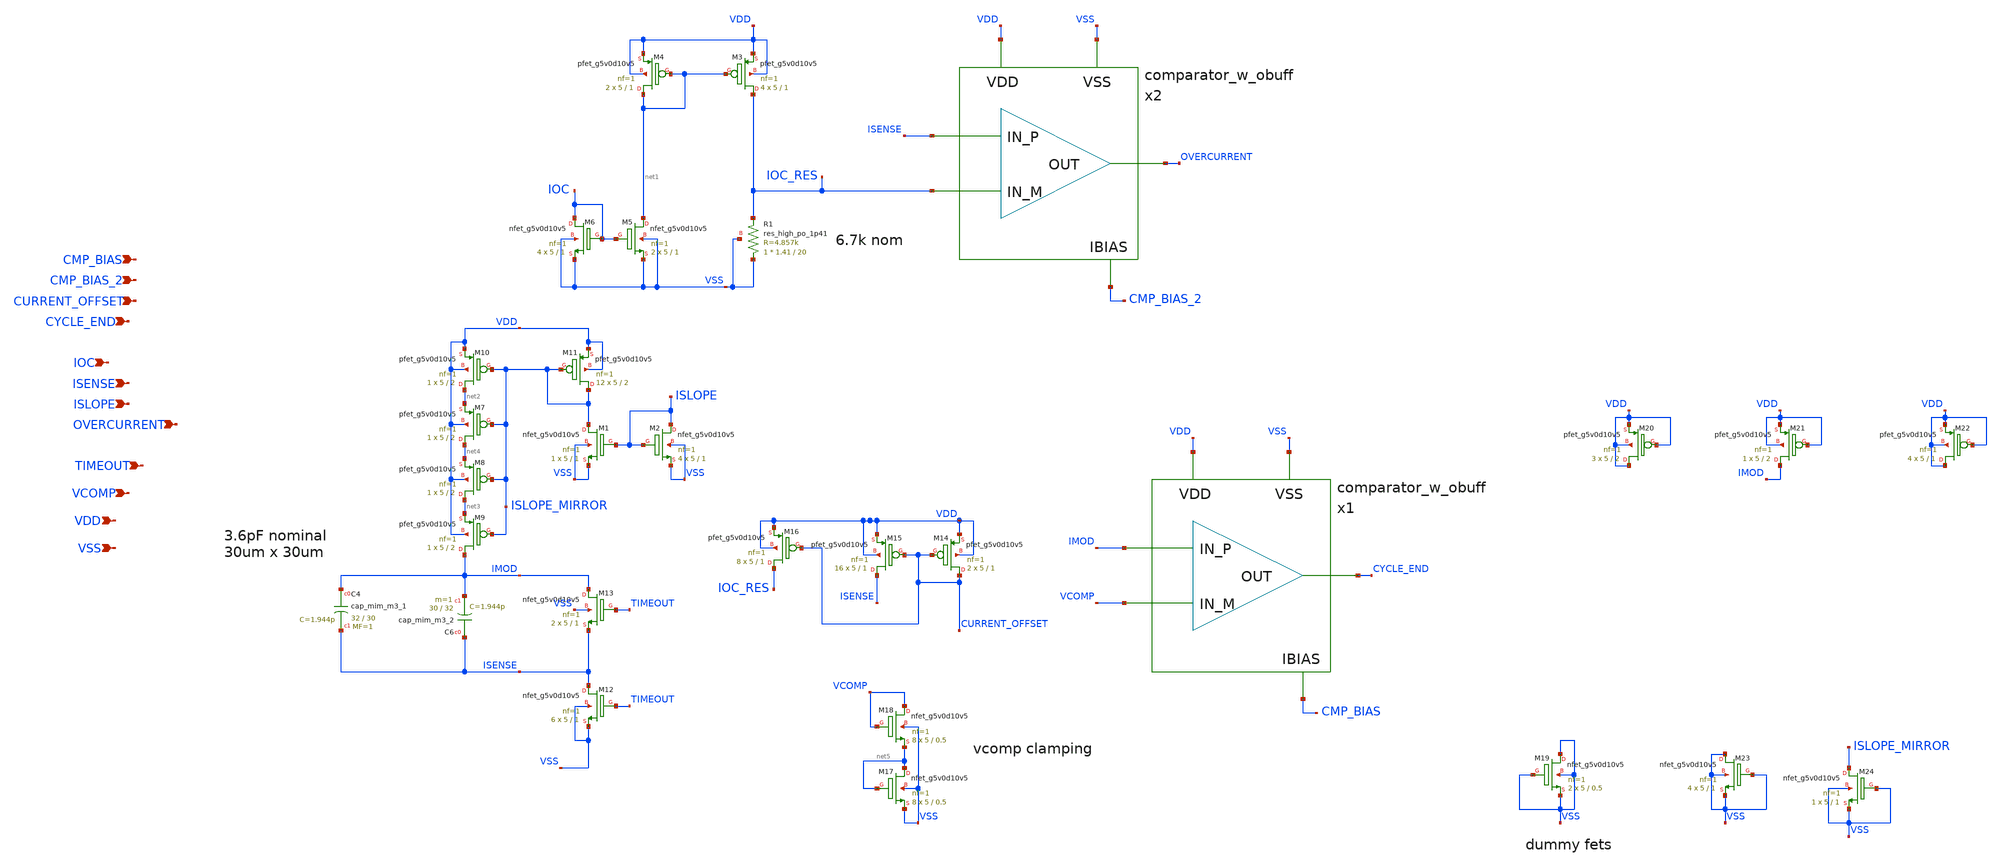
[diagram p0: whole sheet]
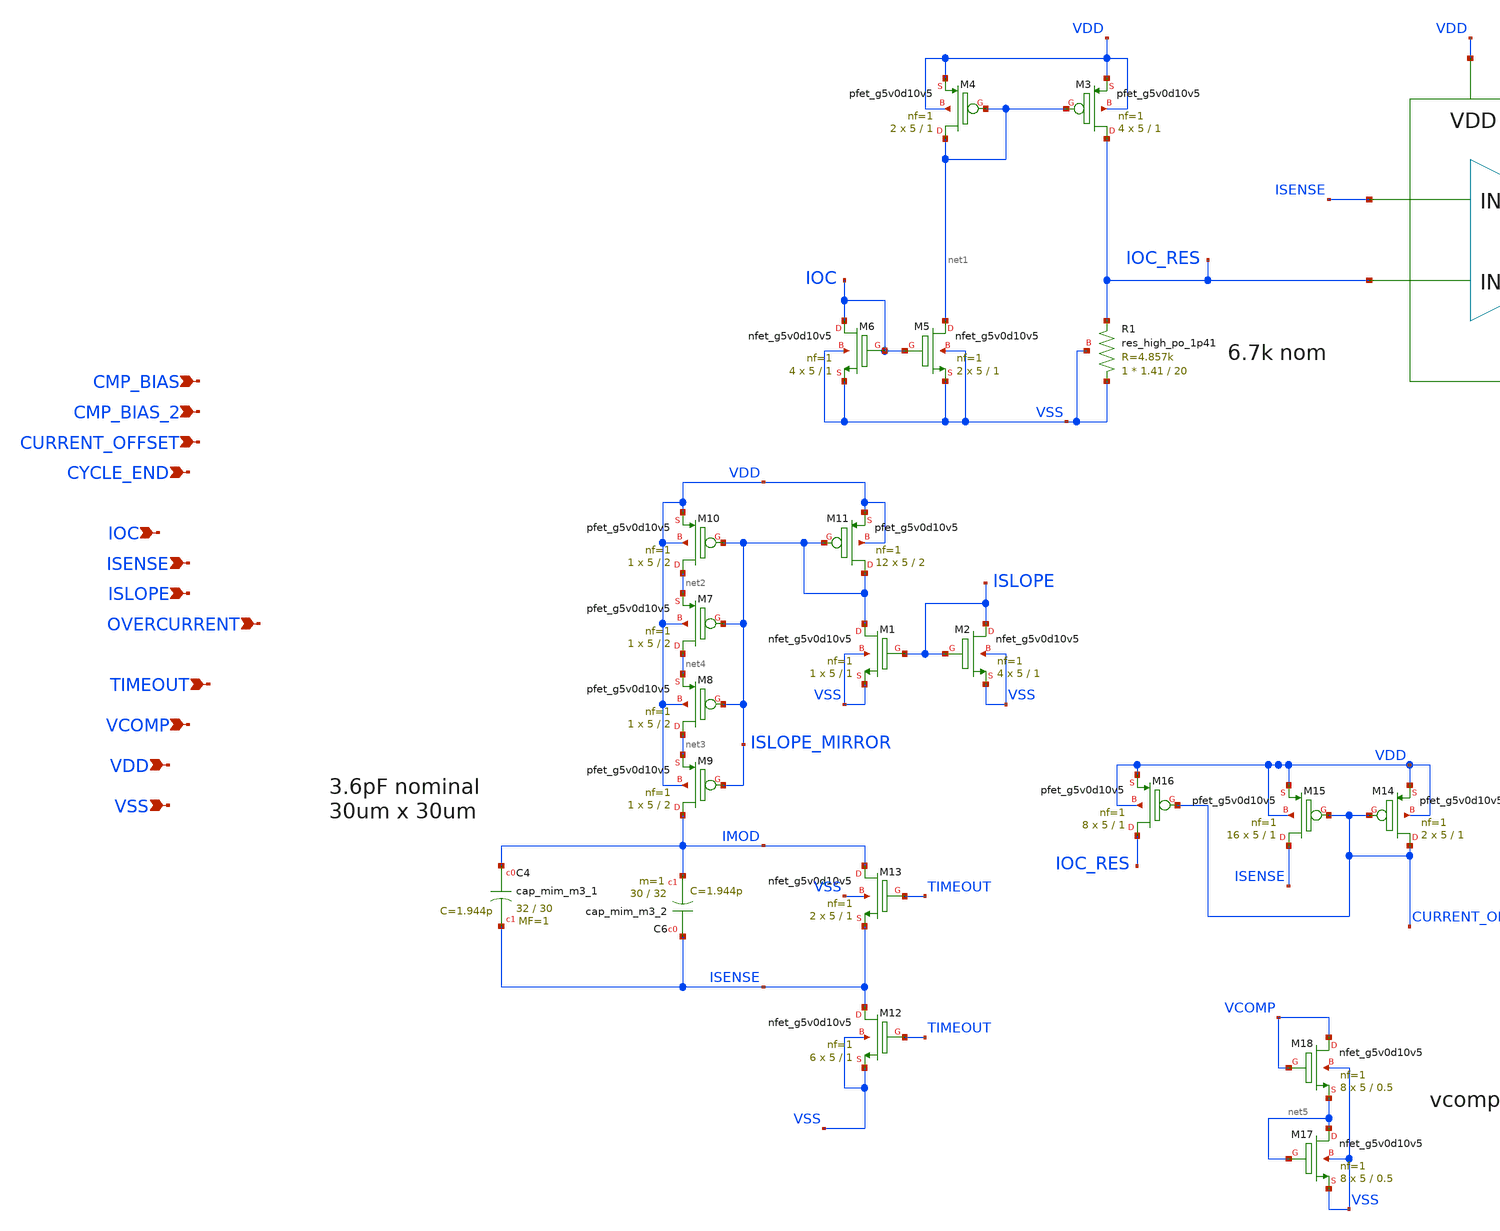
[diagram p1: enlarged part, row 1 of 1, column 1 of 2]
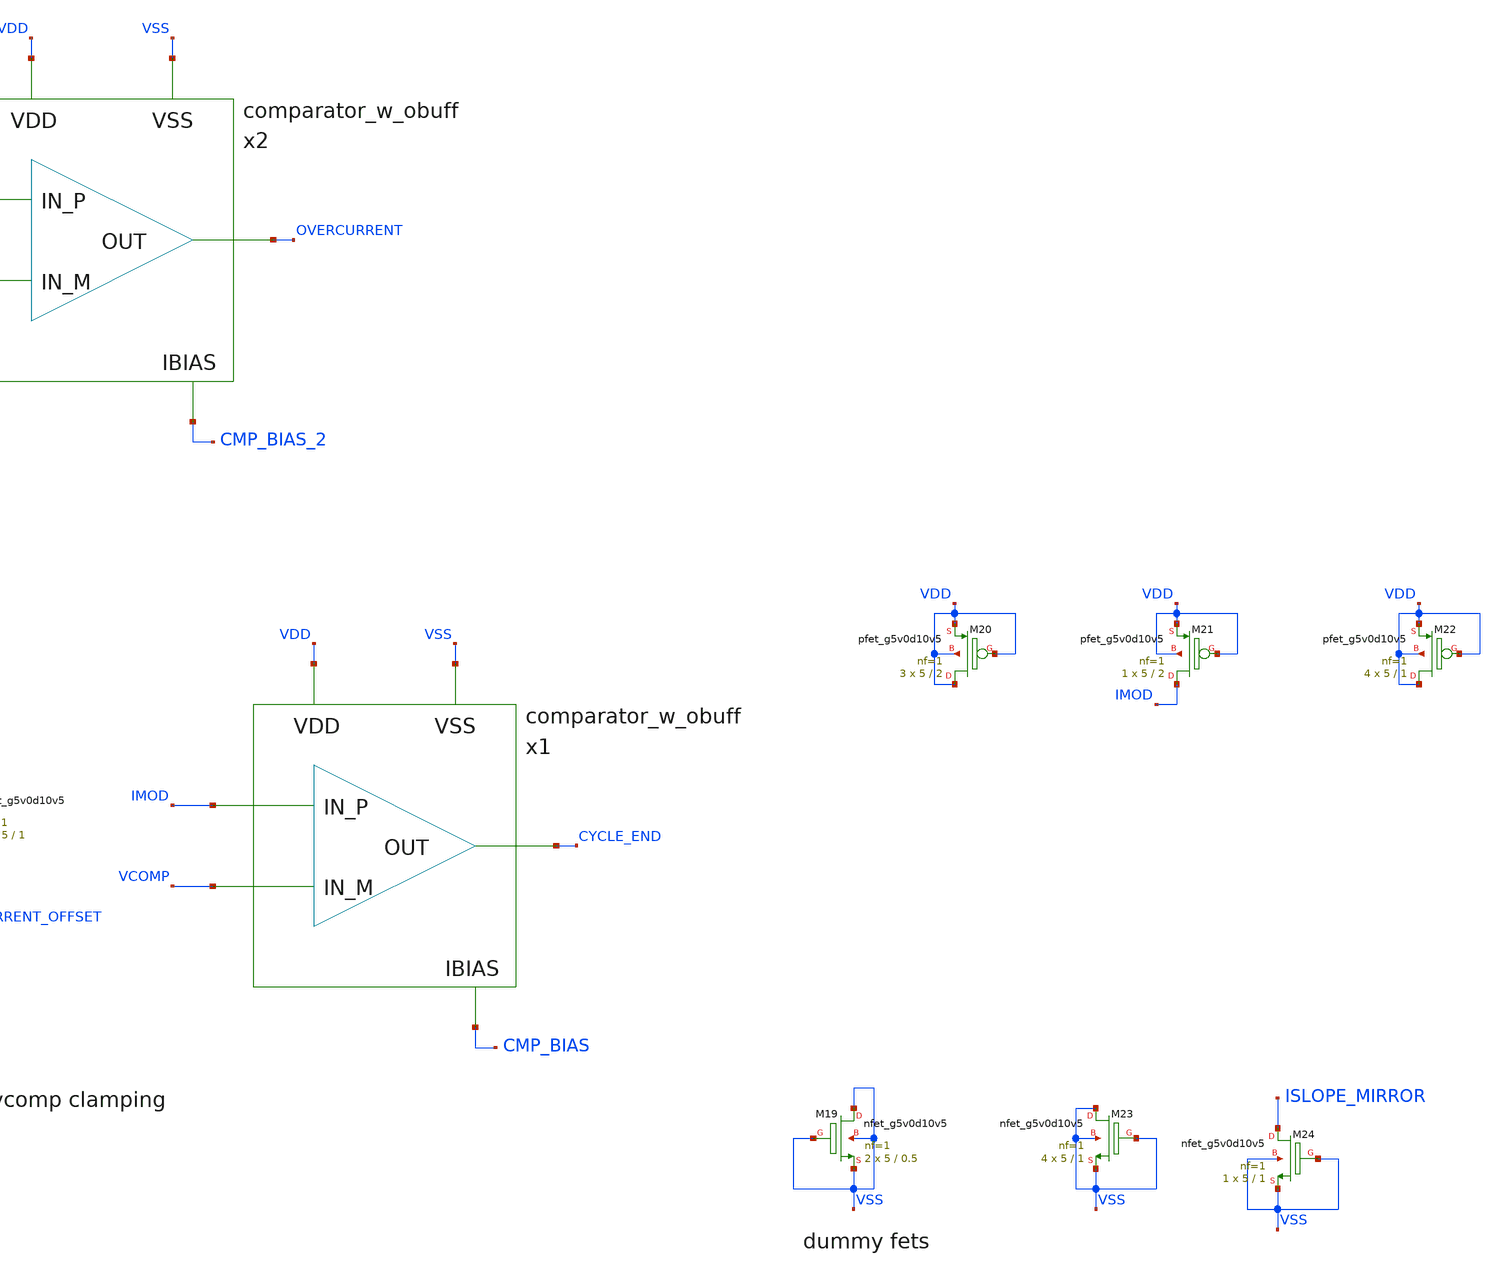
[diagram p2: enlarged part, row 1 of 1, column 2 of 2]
** sch_path: images/iic-osic-tools/addons/examples/open-pmic/design/modulator/modulator.sch
**.subckt modulator CMP_BIAS CMP_BIAS_2 CURRENT_OFFSET CYCLE_END IOC ISENSE ISLOPE OVERCURRENT
*+ TIMEOUT VCOMP VDD VSS
*.ipin CMP_BIAS
*.ipin CMP_BIAS_2
*.ipin CURRENT_OFFSET
*.ipin CYCLE_END
*.ipin IOC
*.ipin ISENSE
*.ipin ISLOPE
*.ipin OVERCURRENT
*.ipin TIMEOUT
*.ipin VCOMP
*.ipin VDD
*.ipin VSS
x1 CMP_BIAS VDD VCOMP IMOD CYCLE_END VSS comparator_w_obuff
XM13 IMOD TIMEOUT ISENSE VSS sky130_fd_pr__nfet_g5v0d10v5 L=1 W=5 nf=1 ad='int((nf+1)/2) * W/nf * 0.29'
+ as='int((nf+2)/2) * W/nf * 0.29' pd='2*int((nf+1)/2) * (W/nf + 0.29)' ps='2*int((nf+2)/2) * (W/nf + 0.29)'
+ nrd='0.29 / W' nrs='0.29 / W' sa=0 sb=0 sd=0 mult=2 m=2
XC4 IMOD ISENSE sky130_fd_pr__cap_mim_m3_1 W=32 L=30 MF=1 m=1
XC6 ISENSE IMOD sky130_fd_pr__cap_mim_m3_2 W=30 L=32 MF=1 m=1
XM1 ISLOPE_MIRROR ISLOPE VSS VSS sky130_fd_pr__nfet_g5v0d10v5 L=1 W=5 nf=1 ad='int((nf+1)/2) * W/nf * 0.29'
+ as='int((nf+2)/2) * W/nf * 0.29' pd='2*int((nf+1)/2) * (W/nf + 0.29)' ps='2*int((nf+2)/2) * (W/nf + 0.29)'
+ nrd='0.29 / W' nrs='0.29 / W' sa=0 sb=0 sd=0 mult=1 m=1
XM2 ISLOPE ISLOPE VSS VSS sky130_fd_pr__nfet_g5v0d10v5 L=1 W=5 nf=1 ad='int((nf+1)/2) * W/nf * 0.29'
+ as='int((nf+2)/2) * W/nf * 0.29' pd='2*int((nf+1)/2) * (W/nf + 0.29)' ps='2*int((nf+2)/2) * (W/nf + 0.29)'
+ nrd='0.29 / W' nrs='0.29 / W' sa=0 sb=0 sd=0 mult=4 m=4
x2 CMP_BIAS_2 VDD IOC_RES ISENSE OVERCURRENT VSS comparator_w_obuff
XM12 ISENSE TIMEOUT VSS VSS sky130_fd_pr__nfet_g5v0d10v5 L=1 W=5 nf=1 ad='int((nf+1)/2) * W/nf * 0.29'
+ as='int((nf+2)/2) * W/nf * 0.29' pd='2*int((nf+1)/2) * (W/nf + 0.29)' ps='2*int((nf+2)/2) * (W/nf + 0.29)'
+ nrd='0.29 / W' nrs='0.29 / W' sa=0 sb=0 sd=0 mult=6 m=6
XR1 VSS IOC_RES VSS sky130_fd_pr__res_high_po_1p41 L=20 mult=1 m=1
XM3 IOC_RES net1 VDD VDD sky130_fd_pr__pfet_g5v0d10v5 L=1 W=5 nf=1 ad='int((nf+1)/2) * W/nf * 0.29' as='int((nf+2)/2) * W/nf * 0.29'
+ pd='2*int((nf+1)/2) * (W/nf + 0.29)' ps='2*int((nf+2)/2) * (W/nf + 0.29)' nrd='0.29 / W' nrs='0.29 / W'
+ sa=0 sb=0 sd=0 mult=4 m=4
XM4 net1 net1 VDD VDD sky130_fd_pr__pfet_g5v0d10v5 L=1 W=5 nf=1 ad='int((nf+1)/2) * W/nf * 0.29' as='int((nf+2)/2) * W/nf * 0.29'
+ pd='2*int((nf+1)/2) * (W/nf + 0.29)' ps='2*int((nf+2)/2) * (W/nf + 0.29)' nrd='0.29 / W' nrs='0.29 / W'
+ sa=0 sb=0 sd=0 mult=2 m=2
XM10 net2 ISLOPE_MIRROR VDD VDD sky130_fd_pr__pfet_g5v0d10v5 L=2 W=5 nf=1 ad='int((nf+1)/2) * W/nf * 0.29'
+ as='int((nf+2)/2) * W/nf * 0.29' pd='2*int((nf+1)/2) * (W/nf + 0.29)' ps='2*int((nf+2)/2) * (W/nf + 0.29)'
+ nrd='0.29 / W' nrs='0.29 / W' sa=0 sb=0 sd=0 mult=1 m=1
XM5 net1 IOC VSS VSS sky130_fd_pr__nfet_g5v0d10v5 L=1 W=5 nf=1 ad='int((nf+1)/2) * W/nf * 0.29' as='int((nf+2)/2) * W/nf * 0.29'
+ pd='2*int((nf+1)/2) * (W/nf + 0.29)' ps='2*int((nf+2)/2) * (W/nf + 0.29)' nrd='0.29 / W' nrs='0.29 / W'
+ sa=0 sb=0 sd=0 mult=2 m=2
XM6 IOC IOC VSS VSS sky130_fd_pr__nfet_g5v0d10v5 L=1 W=5 nf=1 ad='int((nf+1)/2) * W/nf * 0.29' as='int((nf+2)/2) * W/nf * 0.29'
+ pd='2*int((nf+1)/2) * (W/nf + 0.29)' ps='2*int((nf+2)/2) * (W/nf + 0.29)' nrd='0.29 / W' nrs='0.29 / W'
+ sa=0 sb=0 sd=0 mult=4 m=4
XM7 net4 ISLOPE_MIRROR net2 VDD sky130_fd_pr__pfet_g5v0d10v5 L=2 W=5 nf=1 ad='int((nf+1)/2) * W/nf * 0.29'
+ as='int((nf+2)/2) * W/nf * 0.29' pd='2*int((nf+1)/2) * (W/nf + 0.29)' ps='2*int((nf+2)/2) * (W/nf + 0.29)'
+ nrd='0.29 / W' nrs='0.29 / W' sa=0 sb=0 sd=0 mult=1 m=1
XM8 net3 ISLOPE_MIRROR net4 VDD sky130_fd_pr__pfet_g5v0d10v5 L=2 W=5 nf=1 ad='int((nf+1)/2) * W/nf * 0.29'
+ as='int((nf+2)/2) * W/nf * 0.29' pd='2*int((nf+1)/2) * (W/nf + 0.29)' ps='2*int((nf+2)/2) * (W/nf + 0.29)'
+ nrd='0.29 / W' nrs='0.29 / W' sa=0 sb=0 sd=0 mult=1 m=1
XM9 IMOD ISLOPE_MIRROR net3 VDD sky130_fd_pr__pfet_g5v0d10v5 L=2 W=5 nf=1 ad='int((nf+1)/2) * W/nf * 0.29'
+ as='int((nf+2)/2) * W/nf * 0.29' pd='2*int((nf+1)/2) * (W/nf + 0.29)' ps='2*int((nf+2)/2) * (W/nf + 0.29)'
+ nrd='0.29 / W' nrs='0.29 / W' sa=0 sb=0 sd=0 mult=1 m=1
XM11 ISLOPE_MIRROR ISLOPE_MIRROR VDD VDD sky130_fd_pr__pfet_g5v0d10v5 L=2 W=5 nf=1 ad='int((nf+1)/2) * W/nf * 0.29'
+ as='int((nf+2)/2) * W/nf * 0.29' pd='2*int((nf+1)/2) * (W/nf + 0.29)' ps='2*int((nf+2)/2) * (W/nf + 0.29)'
+ nrd='0.29 / W' nrs='0.29 / W' sa=0 sb=0 sd=0 mult=12 m=12
XM14 CURRENT_OFFSET CURRENT_OFFSET VDD VDD sky130_fd_pr__pfet_g5v0d10v5 L=1 W=5 nf=1 ad='int((nf+1)/2) * W/nf * 0.29'
+ as='int((nf+2)/2) * W/nf * 0.29' pd='2*int((nf+1)/2) * (W/nf + 0.29)' ps='2*int((nf+2)/2) * (W/nf + 0.29)'
+ nrd='0.29 / W' nrs='0.29 / W' sa=0 sb=0 sd=0 mult=2 m=2
XM15 ISENSE CURRENT_OFFSET VDD VDD sky130_fd_pr__pfet_g5v0d10v5 L=1 W=5 nf=1 ad='int((nf+1)/2) * W/nf * 0.29'
+ as='int((nf+2)/2) * W/nf * 0.29' pd='2*int((nf+1)/2) * (W/nf + 0.29)' ps='2*int((nf+2)/2) * (W/nf + 0.29)'
+ nrd='0.29 / W' nrs='0.29 / W' sa=0 sb=0 sd=0 mult=16 m=16
XM16 IOC_RES CURRENT_OFFSET VDD VDD sky130_fd_pr__pfet_g5v0d10v5 L=1 W=5 nf=1 ad='int((nf+1)/2) * W/nf * 0.29'
+ as='int((nf+2)/2) * W/nf * 0.29' pd='2*int((nf+1)/2) * (W/nf + 0.29)' ps='2*int((nf+2)/2) * (W/nf + 0.29)'
+ nrd='0.29 / W' nrs='0.29 / W' sa=0 sb=0 sd=0 mult=8 m=8
XM17 net5 net5 VSS VSS sky130_fd_pr__nfet_g5v0d10v5 L=0.5 W=5 nf=1 ad='int((nf+1)/2) * W/nf * 0.29' as='int((nf+2)/2) * W/nf * 0.29'
+ pd='2*int((nf+1)/2) * (W/nf + 0.29)' ps='2*int((nf+2)/2) * (W/nf + 0.29)' nrd='0.29 / W' nrs='0.29 / W'
+ sa=0 sb=0 sd=0 mult=8 m=8
XM18 VCOMP VCOMP net5 VSS sky130_fd_pr__nfet_g5v0d10v5 L=0.5 W=5 nf=1 ad='int((nf+1)/2) * W/nf * 0.29'
+ as='int((nf+2)/2) * W/nf * 0.29' pd='2*int((nf+1)/2) * (W/nf + 0.29)' ps='2*int((nf+2)/2) * (W/nf + 0.29)'
+ nrd='0.29 / W' nrs='0.29 / W' sa=0 sb=0 sd=0 mult=8 m=8
XM19 VSS VSS VSS VSS sky130_fd_pr__nfet_g5v0d10v5 L=0.5 W=5 nf=1 ad='int((nf+1)/2) * W/nf * 0.29' as='int((nf+2)/2) * W/nf * 0.29'
+ pd='2*int((nf+1)/2) * (W/nf + 0.29)' ps='2*int((nf+2)/2) * (W/nf + 0.29)' nrd='0.29 / W' nrs='0.29 / W'
+ sa=0 sb=0 sd=0 mult=2 m=2
XM20 VDD VDD VDD VDD sky130_fd_pr__pfet_g5v0d10v5 L=2 W=5 nf=1 ad='int((nf+1)/2) * W/nf * 0.29' as='int((nf+2)/2) * W/nf * 0.29'
+ pd='2*int((nf+1)/2) * (W/nf + 0.29)' ps='2*int((nf+2)/2) * (W/nf + 0.29)' nrd='0.29 / W' nrs='0.29 / W'
+ sa=0 sb=0 sd=0 mult=3 m=3
XM21 IMOD VDD VDD VDD sky130_fd_pr__pfet_g5v0d10v5 L=2 W=5 nf=1 ad='int((nf+1)/2) * W/nf * 0.29' as='int((nf+2)/2) * W/nf * 0.29'
+ pd='2*int((nf+1)/2) * (W/nf + 0.29)' ps='2*int((nf+2)/2) * (W/nf + 0.29)' nrd='0.29 / W' nrs='0.29 / W'
+ sa=0 sb=0 sd=0 mult=1 m=1
XM22 VDD VDD VDD VDD sky130_fd_pr__pfet_g5v0d10v5 L=1 W=5 nf=1 ad='int((nf+1)/2) * W/nf * 0.29' as='int((nf+2)/2) * W/nf * 0.29'
+ pd='2*int((nf+1)/2) * (W/nf + 0.29)' ps='2*int((nf+2)/2) * (W/nf + 0.29)' nrd='0.29 / W' nrs='0.29 / W'
+ sa=0 sb=0 sd=0 mult=4 m=4
XM23 VSS VSS VSS VSS sky130_fd_pr__nfet_g5v0d10v5 L=1 W=5 nf=1 ad='int((nf+1)/2) * W/nf * 0.29' as='int((nf+2)/2) * W/nf * 0.29'
+ pd='2*int((nf+1)/2) * (W/nf + 0.29)' ps='2*int((nf+2)/2) * (W/nf + 0.29)' nrd='0.29 / W' nrs='0.29 / W'
+ sa=0 sb=0 sd=0 mult=4 m=4
XM24 ISLOPE_MIRROR VSS VSS VSS sky130_fd_pr__nfet_g5v0d10v5 L=1 W=5 nf=1 ad='int((nf+1)/2) * W/nf * 0.29'
+ as='int((nf+2)/2) * W/nf * 0.29' pd='2*int((nf+1)/2) * (W/nf + 0.29)' ps='2*int((nf+2)/2) * (W/nf + 0.29)'
+ nrd='0.29 / W' nrs='0.29 / W' sa=0 sb=0 sd=0 mult=1 m=1
**.ends
.end
